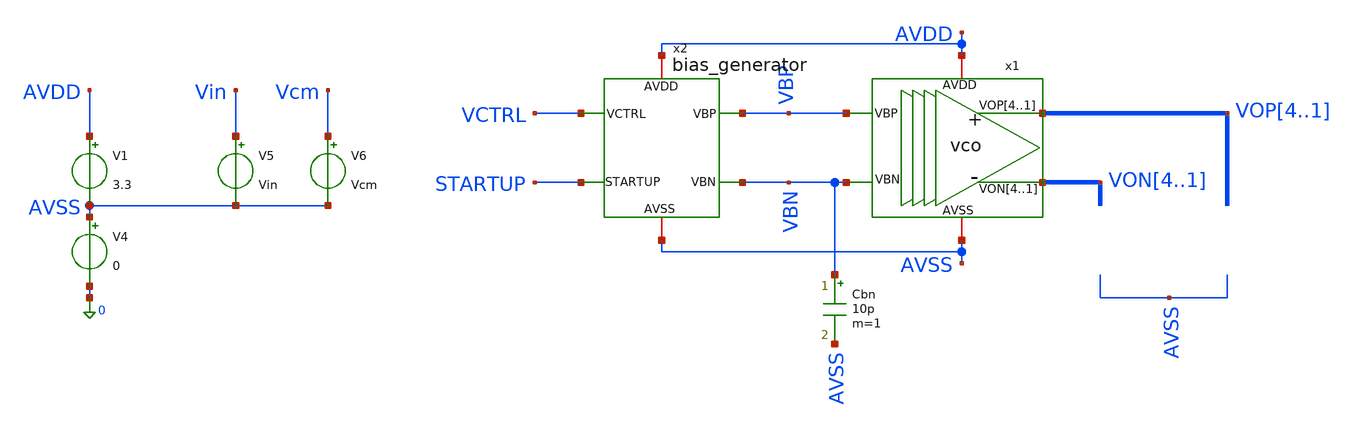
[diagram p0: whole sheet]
** sch_path: designs/libs/tb_analog/tb_vco/tb_vco.sch
**.subckt tb_vco
x1 VOP4 VOP3 VOP2 VOP1 VON4 VON3 VON2 VON1 AVDD AVSS VBP VBN vco
V1 AVDD AVSS 3.3
V4 AVSS 0 0
V5 Vin AVSS Vin
V6 Vcm AVSS Vcm
x2 VCTRL AVDD STARTUP AVSS VBP VBN bias_generator
Cbn VBN AVSS 10p m=1
**** begin user architecture code


.param vbp=2.1 vbn=1.2 Vin=0 Vcm=2.5
.ic v(vop1)=3.3 v(von1)=0 v(startup)=0
.param t1=1u t2=2u t3=3u t4=4u t5=5u t6=6u t7=7u t8=8u tr=100n

.param d0=0 d1=0.4125 d2=0.825 d3=1.2375 d4=1.65 d5=2.0625 d6=2.475 d7=2.8875 d8=3.3

vs startup 0 pulse(0 1 100n 10n 10n 100n 100u)
vctrl vctrl 0 pwl( 0 d1 t1 d1 't1+tr' d8 t2 d8 't2+tr' d7 t3 d7 't3+tr' d6 t4 d6 't4+tr' d5 t5 d5 't5+tr'
+ d4 t6 d4 't6+tr' d3 t7 d3 't7+tr' d2 t8 d2 't8+tr' d1 R 0)

.control
save all

OP
show all

tran 100p 10u
*DC V5 -1 1 0.01
*TRAN 10u

let sum = v(VOP1) + v(VON1)
let diff = v(VOP1) - v(VON1)
*let gain = deriv(diff)
let vcm = AVG(sum/2)


meas tran vmax MAX v(VOP1) FROM=10n TO=20n
meas tran vmin MIN v(VOP1) FROM=10n TO=20n
let vswing = vmax-vmin

write tb_vco.raw
.endc



.include $::180MCU_MODELS/design.ngspice
.lib $::180MCU_MODELS/sm141064.ngspice typical
*.lib $::180MCU_MODELS/sm141064.ngspice SS
*.lib $::180MCU_MODELS/sm141064.ngspice FF
*.lib $::180MCU_MODELS/sm141064.ngspice SF
*.lib $::180MCU_MODELS/sm141064.ngspice FS

**** end user architecture code
**.ends

* expanding   symbol:  libs/core_analog/vco/vco.sym # of pins=6
** sym_path: designs/libs/core_analog/vco/vco.sym
** sch_path: designs/libs/core_analog/vco/vco.sch
.subckt vco VOP4 VOP3 VOP2 VOP1 VON4 VON3 VON2 VON1 AVDD AVSS VBP VBN
*.opin VOP4,VOP3,VOP2,VOP1
*.opin VON4,VON3,VON2,VON1
*.ipin VBP
*.ipin VBN
*.iopin AVDD
*.iopin AVSS
x1 VOP1 AVDD VOP4 VON4 VON1 AVSS VBP VBN delay_stage
x2 VOP2 AVDD VON1 VOP1 VON2 AVSS VBP VBN delay_stage
x3 VOP3 AVDD VON2 VOP2 VON3 AVSS VBP VBN delay_stage
x4 VOP4 AVDD VON3 VOP3 VON4 AVSS VBP VBN delay_stage
.ends


* expanding   symbol:  libs/core_analog/bias_generator/bias_generator.sym # of pins=6
** sym_path: designs/libs/core_analog/bias_generator/bias_generator.sym
** sch_path: designs/libs/core_analog/bias_generator/bias_generator.sch
.subckt bias_generator VCTRL AVDD STARTUP AVSS VBP VBN
*.ipin VCTRL
*.ipin STARTUP
*.iopin AVDD
*.iopin AVSS
*.opin VBP
*.opin VBN
x1 VBN AVDD net2 VCTRL AVSS net1 ota_5t
XM1 net1 net1 AVDD AVDD pfet_03v3 L=0.5u W=8.3u nf=1 ad='int((nf+1)/2) * W/nf * 0.18u' as='int((nf+2)/2) * W/nf * 0.18u'
+ pd='2*int((nf+1)/2) * (W/nf + 0.18u)' ps='2*int((nf+2)/2) * (W/nf + 0.18u)' nrd='0.18u / W' nrs='0.18u / W'
+ sa=0 sb=0 sd=0 m=16
Vmeas net6 net3 0
.save i(vmeas)
Vmeas1 net7 net5 0
.save i(vmeas1)
Vmeas2 net8 net4 0
.save i(vmeas2)
XM10 net5 VBN AVSS AVSS nfet_03v3 L=1u W=37.7u nf=1 ad='int((nf+1)/2) * W/nf * 0.18u' as='int((nf+2)/2) * W/nf * 0.18u'
+ pd='2*int((nf+1)/2) * (W/nf + 0.18u)' ps='2*int((nf+2)/2) * (W/nf + 0.18u)' nrd='0.18u / W' nrs='0.18u / W'
+ sa=0 sb=0 sd=0 m=10
XM5 net2 VCTRL AVDD AVDD pfet_03v3 L=1u W=0.74u nf=1 ad='int((nf+1)/2) * W/nf * 0.18u' as='int((nf+2)/2) * W/nf * 0.18u'
+ pd='2*int((nf+1)/2) * (W/nf + 0.18u)' ps='2*int((nf+2)/2) * (W/nf + 0.18u)' nrd='0.18u / W' nrs='0.18u / W'
+ sa=0 sb=0 sd=0 m=10
XM9 net2 AVDD net7 AVSS nfet_03v3 L=0.8u W=2.6u nf=1 ad='int((nf+1)/2) * W/nf * 0.18u' as='int((nf+2)/2) * W/nf * 0.18u'
+ pd='2*int((nf+1)/2) * (W/nf + 0.18u)' ps='2*int((nf+2)/2) * (W/nf + 0.18u)' nrd='0.18u / W' nrs='0.18u / W'
+ sa=0 sb=0 sd=0 m=10
XM11 VBP AVDD net8 AVSS nfet_03v3 L=0.8u W=2.6u nf=1 ad='int((nf+1)/2) * W/nf * 0.18u' as='int((nf+2)/2) * W/nf * 0.18u'
+ pd='2*int((nf+1)/2) * (W/nf + 0.18u)' ps='2*int((nf+2)/2) * (W/nf + 0.18u)' nrd='0.18u / W' nrs='0.18u / W'
+ sa=0 sb=0 sd=0 m=8
XM6 net2 net2 AVDD AVDD pfet_03v3 L=1u W=0.74u nf=1 ad='int((nf+1)/2) * W/nf * 0.18u' as='int((nf+2)/2) * W/nf * 0.18u'
+ pd='2*int((nf+1)/2) * (W/nf + 0.18u)' ps='2*int((nf+2)/2) * (W/nf + 0.18u)' nrd='0.18u / W' nrs='0.18u / W'
+ sa=0 sb=0 sd=0 m=10
XM7 VBP VBP AVDD AVDD pfet_03v3 L=1u W=0.74u nf=1 ad='int((nf+1)/2) * W/nf * 0.18u' as='int((nf+2)/2) * W/nf * 0.18u'
+ pd='2*int((nf+1)/2) * (W/nf + 0.18u)' ps='2*int((nf+2)/2) * (W/nf + 0.18u)' nrd='0.18u / W' nrs='0.18u / W'
+ sa=0 sb=0 sd=0 m=8
XM8 VBP VBP AVDD AVDD pfet_03v3 L=1u W=0.74u nf=1 ad='int((nf+1)/2) * W/nf * 0.18u' as='int((nf+2)/2) * W/nf * 0.18u'
+ pd='2*int((nf+1)/2) * (W/nf + 0.18u)' ps='2*int((nf+2)/2) * (W/nf + 0.18u)' nrd='0.18u / W' nrs='0.18u / W'
+ sa=0 sb=0 sd=0 m=8
XM2 net1 AVDD net6 AVSS nfet_03v3 L=0.8u W=2.6u nf=1 ad='int((nf+1)/2) * W/nf * 0.18u' as='int((nf+2)/2) * W/nf * 0.18u'
+ pd='2*int((nf+1)/2) * (W/nf + 0.18u)' ps='2*int((nf+2)/2) * (W/nf + 0.18u)' nrd='0.18u / W' nrs='0.18u / W'
+ sa=0 sb=0 sd=0 m=10
XM12 net4 VBN AVSS AVSS nfet_03v3 L=1u W=37.7u nf=1 ad='int((nf+1)/2) * W/nf * 0.18u' as='int((nf+2)/2) * W/nf * 0.18u'
+ pd='2*int((nf+1)/2) * (W/nf + 0.18u)' ps='2*int((nf+2)/2) * (W/nf + 0.18u)' nrd='0.18u / W' nrs='0.18u / W'
+ sa=0 sb=0 sd=0 m=8
XM3 net3 VBN AVSS AVSS nfet_03v3 L=1u W=37.7u nf=1 ad='int((nf+1)/2) * W/nf * 0.18u' as='int((nf+2)/2) * W/nf * 0.18u'
+ pd='2*int((nf+1)/2) * (W/nf + 0.18u)' ps='2*int((nf+2)/2) * (W/nf + 0.18u)' nrd='0.18u / W' nrs='0.18u / W'
+ sa=0 sb=0 sd=0 m=10
XM4 net3 STARTUP AVSS AVSS nfet_03v3 L=1u W=37.7u nf=1 ad='int((nf+1)/2) * W/nf * 0.18u' as='int((nf+2)/2) * W/nf * 0.18u'
+ pd='2*int((nf+1)/2) * (W/nf + 0.18u)' ps='2*int((nf+2)/2) * (W/nf + 0.18u)' nrd='0.18u / W' nrs='0.18u / W'
+ sa=0 sb=0 sd=0 m=10
.ends


* expanding   symbol:  libs/core_analog/delay_stage/delay_stage.sym # of pins=8
** sym_path: designs/libs/core_analog/delay_stage/delay_stage.sym
** sch_path: designs/libs/core_analog/delay_stage/delay_stage.sch
.subckt delay_stage VOP AVDD VIP VIN VON AVSS VBP VBN
*.ipin VIP
*.ipin VIN
*.opin VOP
*.opin VON
*.iopin AVDD
*.iopin AVSS
*.ipin VBP
*.ipin VBN
XM5 VON VIP net1 AVSS nfet_03v3 L=0.5u W=2.08u nf=1 ad='int((nf+1)/2) * W/nf * 0.18u' as='int((nf+2)/2) * W/nf * 0.18u'
+ pd='2*int((nf+1)/2) * (W/nf + 0.18u)' ps='2*int((nf+2)/2) * (W/nf + 0.18u)' nrd='0.18u / W' nrs='0.18u / W'
+ sa=0 sb=0 sd=0 m=8
XM2 VON VON AVDD AVDD pfet_03v3 L=1.5u W=1.1u nf=1 ad='int((nf+1)/2) * W/nf * 0.18u' as='int((nf+2)/2) * W/nf * 0.18u'
+ pd='2*int((nf+1)/2) * (W/nf + 0.18u)' ps='2*int((nf+2)/2) * (W/nf + 0.18u)' nrd='0.18u / W' nrs='0.18u / W'
+ sa=0 sb=0 sd=0 m=8
XM6 VOP VIN net1 AVSS nfet_03v3 L=0.5u W=2.08u nf=1 ad='int((nf+1)/2) * W/nf * 0.18u' as='int((nf+2)/2) * W/nf * 0.18u'
+ pd='2*int((nf+1)/2) * (W/nf + 0.18u)' ps='2*int((nf+2)/2) * (W/nf + 0.18u)' nrd='0.18u / W' nrs='0.18u / W'
+ sa=0 sb=0 sd=0 m=8
XM1 VON VBP AVDD AVDD pfet_03v3 L=1.5u W=1.1u nf=1 ad='int((nf+1)/2) * W/nf * 0.18u' as='int((nf+2)/2) * W/nf * 0.18u'
+ pd='2*int((nf+1)/2) * (W/nf + 0.18u)' ps='2*int((nf+2)/2) * (W/nf + 0.18u)' nrd='0.18u / W' nrs='0.18u / W'
+ sa=0 sb=0 sd=0 m=8
XM3 VOP VBP AVDD AVDD pfet_03v3 L=1.5u W=1.1u nf=1 ad='int((nf+1)/2) * W/nf * 0.18u' as='int((nf+2)/2) * W/nf * 0.18u'
+ pd='2*int((nf+1)/2) * (W/nf + 0.18u)' ps='2*int((nf+2)/2) * (W/nf + 0.18u)' nrd='0.18u / W' nrs='0.18u / W'
+ sa=0 sb=0 sd=0 m=8
XM4 VOP VOP AVDD AVDD pfet_03v3 L=1.5u W=1.1u nf=1 ad='int((nf+1)/2) * W/nf * 0.18u' as='int((nf+2)/2) * W/nf * 0.18u'
+ pd='2*int((nf+1)/2) * (W/nf + 0.18u)' ps='2*int((nf+2)/2) * (W/nf + 0.18u)' nrd='0.18u / W' nrs='0.18u / W'
+ sa=0 sb=0 sd=0 m=8
XM8 net1 VBN AVSS AVSS nfet_03v3 L=0.5u W=11.25u nf=1 ad='int((nf+1)/2) * W/nf * 0.18u' as='int((nf+2)/2) * W/nf * 0.18u'
+ pd='2*int((nf+1)/2) * (W/nf + 0.18u)' ps='2*int((nf+2)/2) * (W/nf + 0.18u)' nrd='0.18u / W' nrs='0.18u / W'
+ sa=0 sb=0 sd=0 m=8
.ends


* expanding   symbol:  libs/core_analog/ota_5t/ota_5t.sym # of pins=6
** sym_path: designs/libs/core_analog/ota_5t/ota_5t.sym
** sch_path: designs/libs/core_analog/ota_5t/ota_5t.sch
.subckt ota_5t VO AVDD VI+ VI- AVSS VB
*.ipin VI+
*.ipin VI-
*.ipin VB
*.iopin AVDD
*.iopin AVSS
*.opin VO
XM1 VO VI- net2 AVDD pfet_03v3 L=0.5u W=6.55u nf=1 ad='int((nf+1)/2) * W/nf * 0.18u' as='int((nf+2)/2) * W/nf * 0.18u'
+ pd='2*int((nf+1)/2) * (W/nf + 0.18u)' ps='2*int((nf+2)/2) * (W/nf + 0.18u)' nrd='0.18u / W' nrs='0.18u / W'
+ sa=0 sb=0 sd=0 m=8
XM4 VO net1 AVSS AVSS nfet_03v3 L=0.5u W=4.8u nf=1 ad='int((nf+1)/2) * W/nf * 0.18u' as='int((nf+2)/2) * W/nf * 0.18u'
+ pd='2*int((nf+1)/2) * (W/nf + 0.18u)' ps='2*int((nf+2)/2) * (W/nf + 0.18u)' nrd='0.18u / W' nrs='0.18u / W'
+ sa=0 sb=0 sd=0 m=4
XM3 net2 VB net3 AVDD pfet_03v3 L=0.5u W=8.3u nf=1 ad='int((nf+1)/2) * W/nf * 0.18u' as='int((nf+2)/2) * W/nf * 0.18u'
+ pd='2*int((nf+1)/2) * (W/nf + 0.18u)' ps='2*int((nf+2)/2) * (W/nf + 0.18u)' nrd='0.18u / W' nrs='0.18u / W'
+ sa=0 sb=0 sd=0 m=16
XM2 net1 VI+ net2 AVDD pfet_03v3 L=0.5u W=6.55u nf=1 ad='int((nf+1)/2) * W/nf * 0.18u' as='int((nf+2)/2) * W/nf * 0.18u'
+ pd='2*int((nf+1)/2) * (W/nf + 0.18u)' ps='2*int((nf+2)/2) * (W/nf + 0.18u)' nrd='0.18u / W' nrs='0.18u / W'
+ sa=0 sb=0 sd=0 m=8
XM5 net1 net1 AVSS AVSS nfet_03v3 L=0.5u W=4.8u nf=1 ad='int((nf+1)/2) * W/nf * 0.18u' as='int((nf+2)/2) * W/nf * 0.18u'
+ pd='2*int((nf+1)/2) * (W/nf + 0.18u)' ps='2*int((nf+2)/2) * (W/nf + 0.18u)' nrd='0.18u / W' nrs='0.18u / W'
+ sa=0 sb=0 sd=0 m=4
Vmeas AVDD net3 0
.save i(vmeas)
.ends

.end
